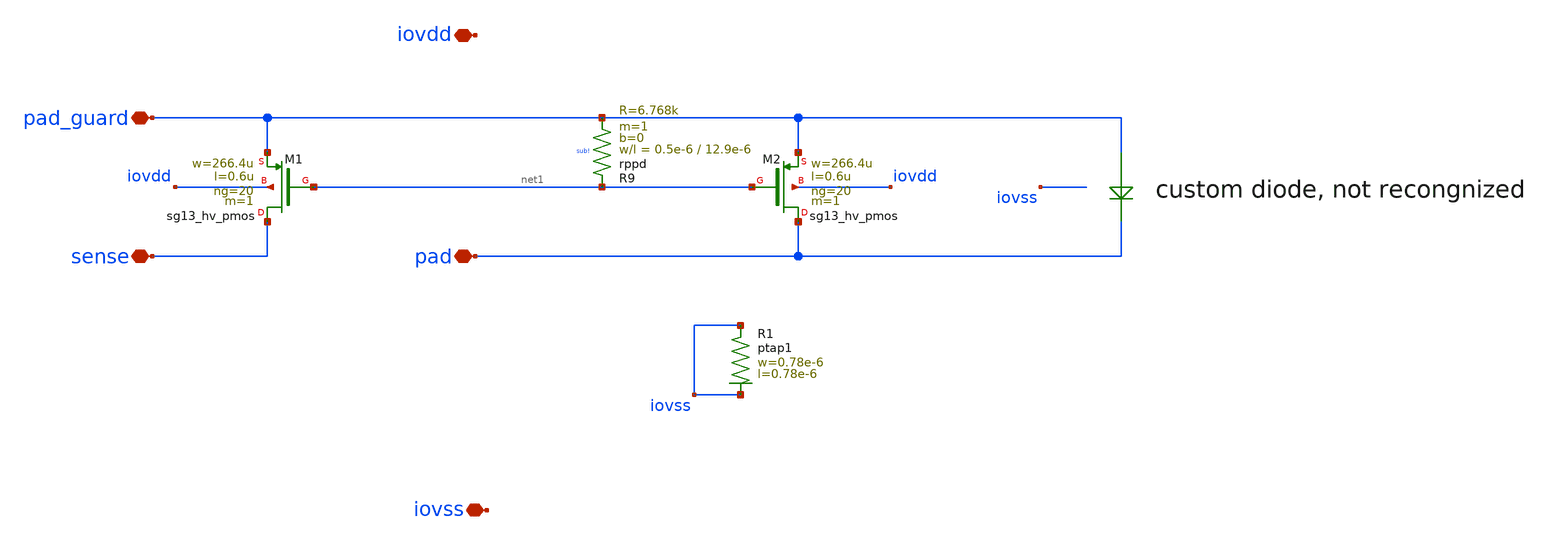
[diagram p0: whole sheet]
** sch_path: trident_test_structures/design_data/xschem/IOPadAnalogGuardLayerSense/pad_guard_to_vdd_first_stage_esd_sense.sch
**.subckt pad_guard_to_vdd_first_stage_esd_sense iovss pad_guard iovdd pad sense
*.iopin iovss
*.iopin pad_guard
*.iopin iovdd
*.iopin pad
*.iopin sense
XR9 net1 pad_guard sub! rppd w=0.5e-6 l=12.9e-6 m=1 b=0 mm_ok=1
XM1 sense net1 pad_guard iovdd sg13_hv_pmos w=266.4u l=0.6u ng=20 m=1 mm_ok=1
XM2 pad net1 pad_guard iovdd sg13_hv_pmos w=266.4u l=0.6u ng=20 m=1 mm_ok=1
XR1 iovss iovss ptap1 R=262.8 w=0.78e-6 l=0.78e-6
**.ends
.end
